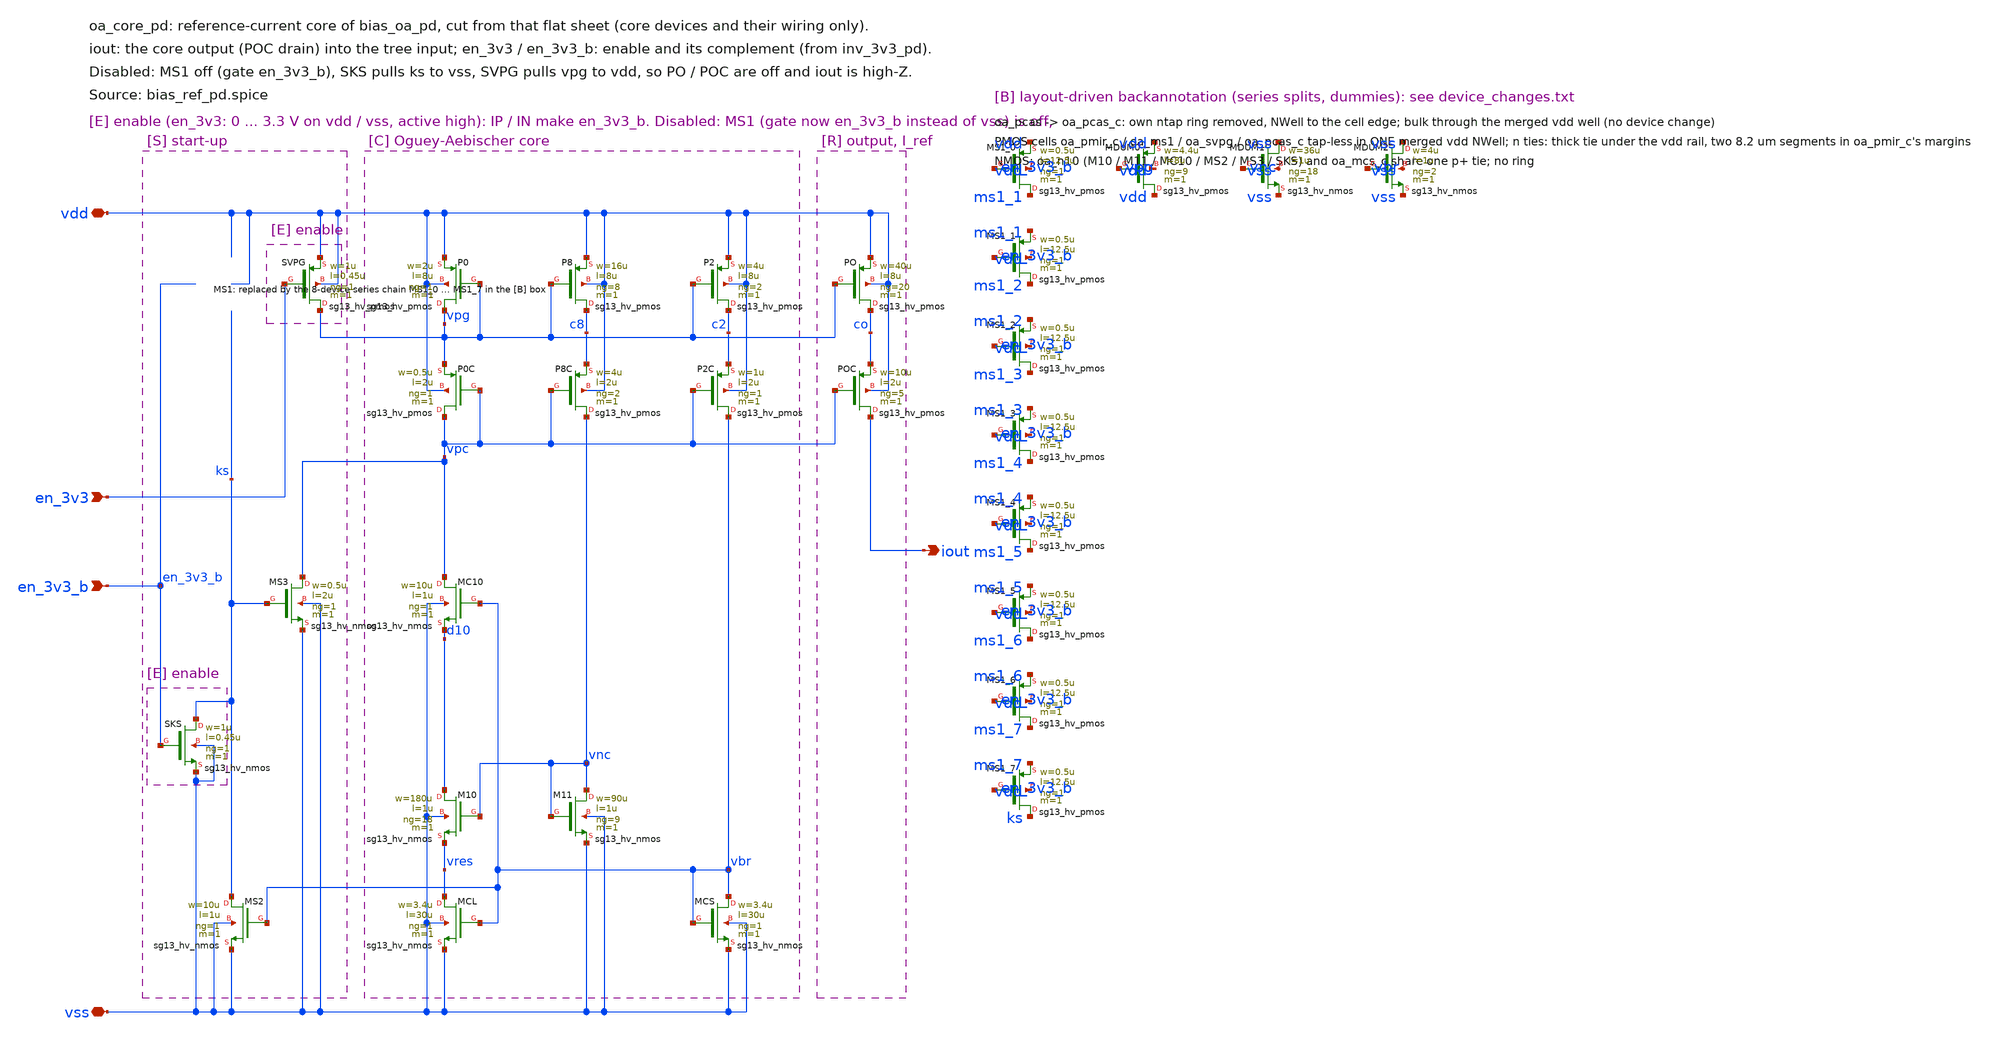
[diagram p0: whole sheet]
** sch_path: sudelbuecher/sg13cmos5l_IOPadDiff2Single_build/agents/A2_oa_core_pd_layout/work_bg/regress_ba/oa_core_pd.sch
**.subckt oa_core_pd vdd vss en_3v3 en_3v3_b iout
*.iopin vdd
*.iopin vss
*.ipin en_3v3
*.ipin en_3v3_b
*.opin iout
XMS2 ks vbr vss vss sg13_hv_nmos w=10u l=1u ng=1 m=1 mm_ok=1
XMS3 vpc ks vss vss sg13_hv_nmos w=0.5u l=2u ng=1 m=1 mm_ok=1
XP0 vpg vpg vdd vdd sg13_hv_pmos w=2u l=8u ng=1 m=1 mm_ok=1
XP0C vpc vpc vpg vdd sg13_hv_pmos w=0.5u l=2u ng=1 m=1 mm_ok=1
XMC10 vpc vbr d10 vss sg13_hv_nmos w=10u l=1u ng=1 m=1 mm_ok=1
XM10 d10 vnc vres vss sg13_hv_nmos w=180u l=1u ng=18 m=1 mm_ok=1
XMCL vres vbr vss vss sg13_hv_nmos w=3.4u l=30u ng=1 m=1 mm_ok=1
XP8 c8 vpg vdd vdd sg13_hv_pmos w=16u l=8u ng=8 m=1 mm_ok=1
XP8C vnc vpc c8 vdd sg13_hv_pmos w=4u l=2u ng=2 m=1 mm_ok=1
XM11 vnc vnc vss vss sg13_hv_nmos w=90u l=1u ng=9 m=1 mm_ok=1
XP2 c2 vpg vdd vdd sg13_hv_pmos w=4u l=8u ng=2 m=1 mm_ok=1
XP2C vbr vpc c2 vdd sg13_hv_pmos w=1u l=2u ng=1 m=1 mm_ok=1
XMCS vbr vbr vss vss sg13_hv_nmos w=3.4u l=30u ng=1 m=1 mm_ok=1
XPO co vpg vdd vdd sg13_hv_pmos w=40u l=8u ng=20 m=1 mm_ok=1
XPOC iout vpc co vdd sg13_hv_pmos w=10u l=2u ng=5 m=1 mm_ok=1
XSKS ks en_3v3_b vss vss sg13_hv_nmos w=1u l=0.45u ng=1 m=1 mm_ok=1
XSVPG vpg en_3v3 vdd vdd sg13_hv_pmos w=1u l=0.45u ng=1 m=1 mm_ok=1
XMS1_0 ms1_1 en_3v3_b vdd vdd sg13_hv_pmos w=0.5u l=12.5u ng=1 m=1 mm_ok=1
XMS1_1 ms1_2 en_3v3_b ms1_1 vdd sg13_hv_pmos w=0.5u l=12.5u ng=1 m=1 mm_ok=1
XMS1_2 ms1_3 en_3v3_b ms1_2 vdd sg13_hv_pmos w=0.5u l=12.5u ng=1 m=1 mm_ok=1
XMS1_3 ms1_4 en_3v3_b ms1_3 vdd sg13_hv_pmos w=0.5u l=12.5u ng=1 m=1 mm_ok=1
XMS1_4 ms1_5 en_3v3_b ms1_4 vdd sg13_hv_pmos w=0.5u l=12.5u ng=1 m=1 mm_ok=1
XMS1_5 ms1_6 en_3v3_b ms1_5 vdd sg13_hv_pmos w=0.5u l=12.5u ng=1 m=1 mm_ok=1
XMS1_6 ms1_7 en_3v3_b ms1_6 vdd sg13_hv_pmos w=0.5u l=12.5u ng=1 m=1 mm_ok=1
XMS1_7 ks en_3v3_b ms1_7 vdd sg13_hv_pmos w=0.5u l=12.5u ng=1 m=1 mm_ok=1
XMDUM0 vdd vpg vdd vdd sg13_hv_pmos w=4.4u l=8u ng=9 m=1 mm_ok=1
XMDUM1 vss vnc vss vss sg13_hv_nmos w=36u l=1u ng=18 m=1 mm_ok=1
XMDUM2 vss vbr vss vss sg13_hv_nmos w=4u l=1u ng=2 m=1 mm_ok=1
**.ends
.end
